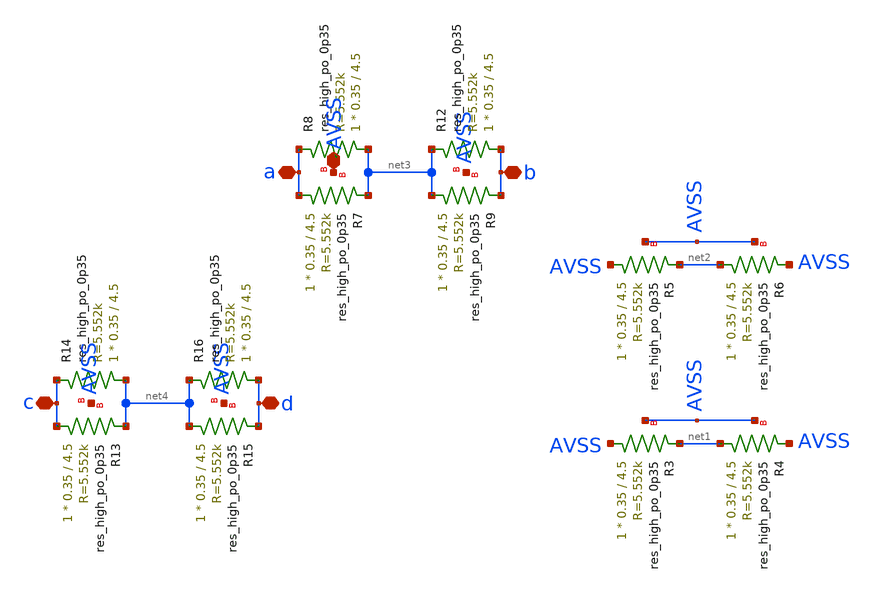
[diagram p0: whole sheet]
** sch_path: magic/resistor_op_tt.sch
**.subckt resistor_op_tt a b AVSS c d
*.iopin a
*.iopin b
*.iopin AVSS
*.iopin c
*.iopin d
XR3 AVSS net1 AVSS sky130_fd_pr__res_high_po_0p35 L=4.5 mult=1 m=1
XR4 net1 AVSS AVSS sky130_fd_pr__res_high_po_0p35 L=4.5 mult=1 m=1
XR5 AVSS net2 AVSS sky130_fd_pr__res_high_po_0p35 L=4.5 mult=1 m=1
XR6 net2 AVSS AVSS sky130_fd_pr__res_high_po_0p35 L=4.5 mult=1 m=1
XR7 a net3 AVSS sky130_fd_pr__res_high_po_0p35 L=4.5 mult=1 m=1
XR8 net3 a AVSS sky130_fd_pr__res_high_po_0p35 L=4.5 mult=1 m=1
XR9 net3 b AVSS sky130_fd_pr__res_high_po_0p35 L=4.5 mult=1 m=1
XR12 b net3 AVSS sky130_fd_pr__res_high_po_0p35 L=4.5 mult=1 m=1
XR13 c net4 AVSS sky130_fd_pr__res_high_po_0p35 L=4.5 mult=1 m=1
XR14 net4 c AVSS sky130_fd_pr__res_high_po_0p35 L=4.5 mult=1 m=1
XR15 net4 d AVSS sky130_fd_pr__res_high_po_0p35 L=4.5 mult=1 m=1
XR16 d net4 AVSS sky130_fd_pr__res_high_po_0p35 L=4.5 mult=1 m=1
**.ends
.end
